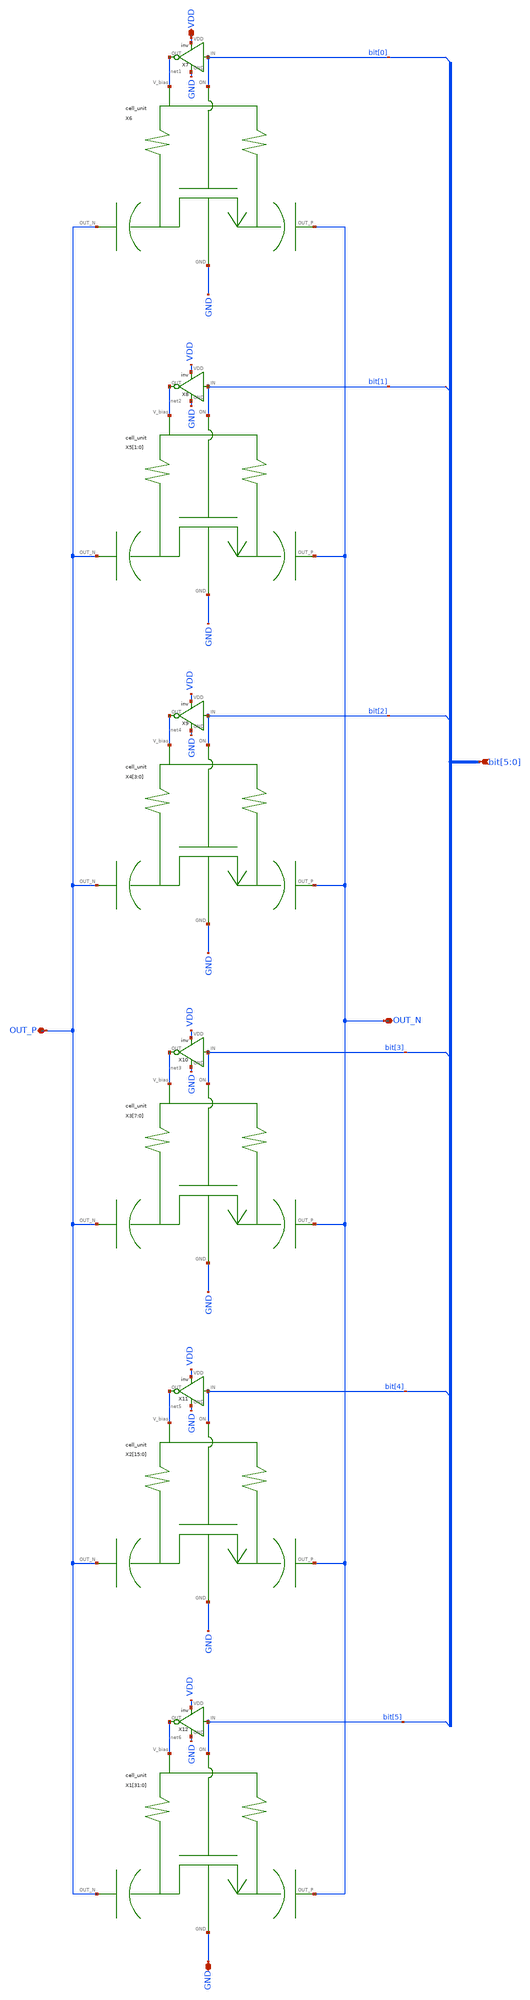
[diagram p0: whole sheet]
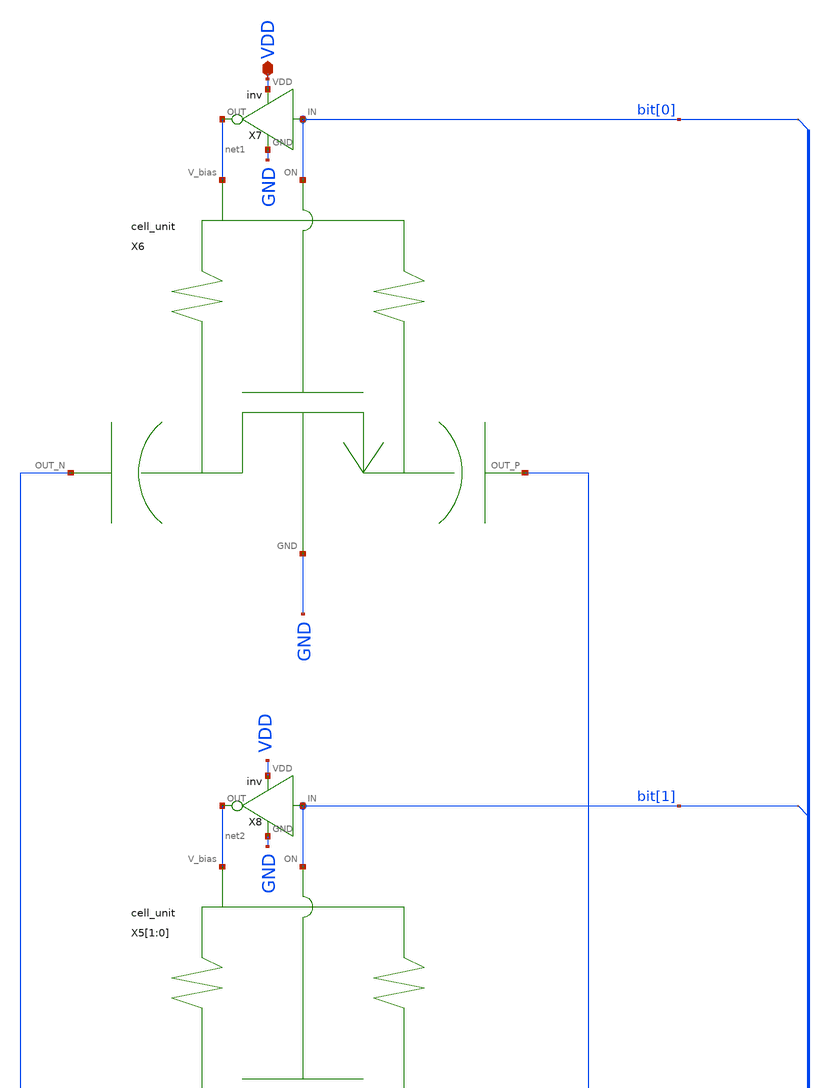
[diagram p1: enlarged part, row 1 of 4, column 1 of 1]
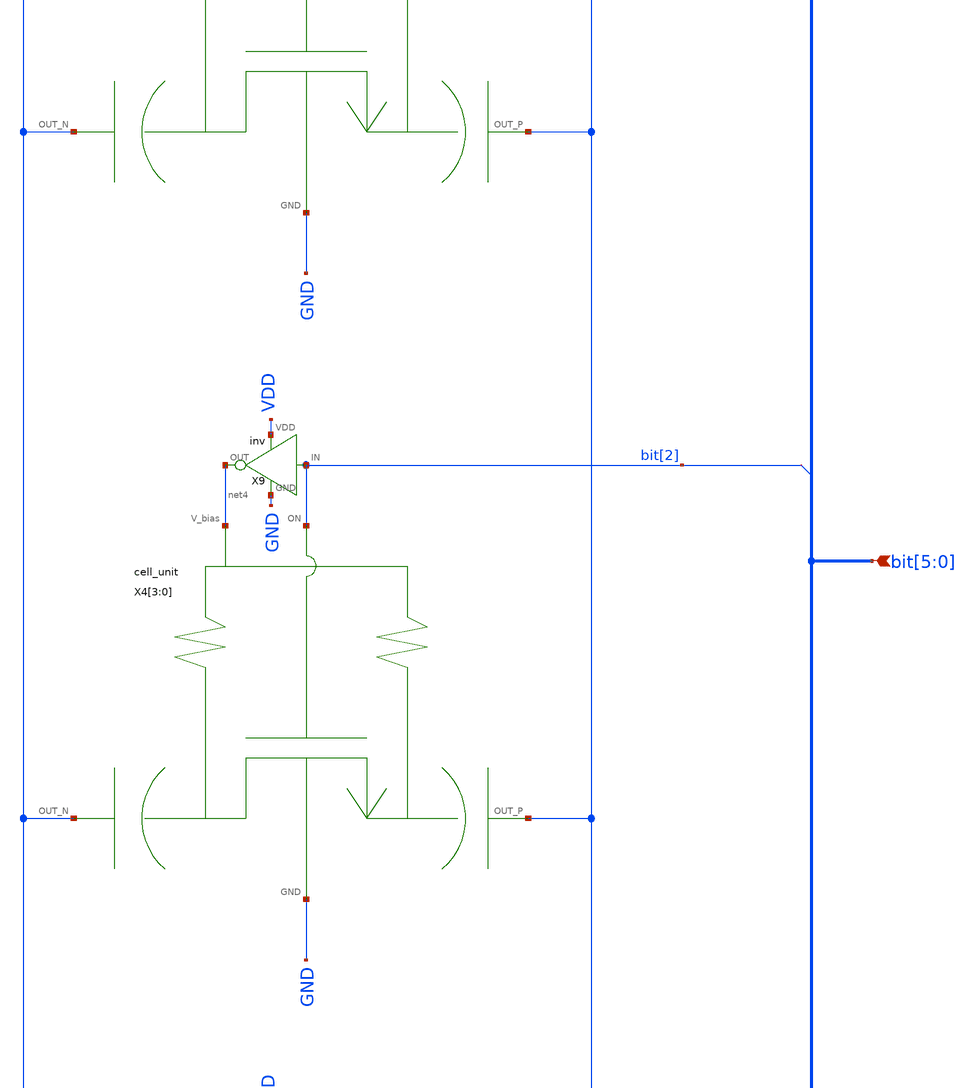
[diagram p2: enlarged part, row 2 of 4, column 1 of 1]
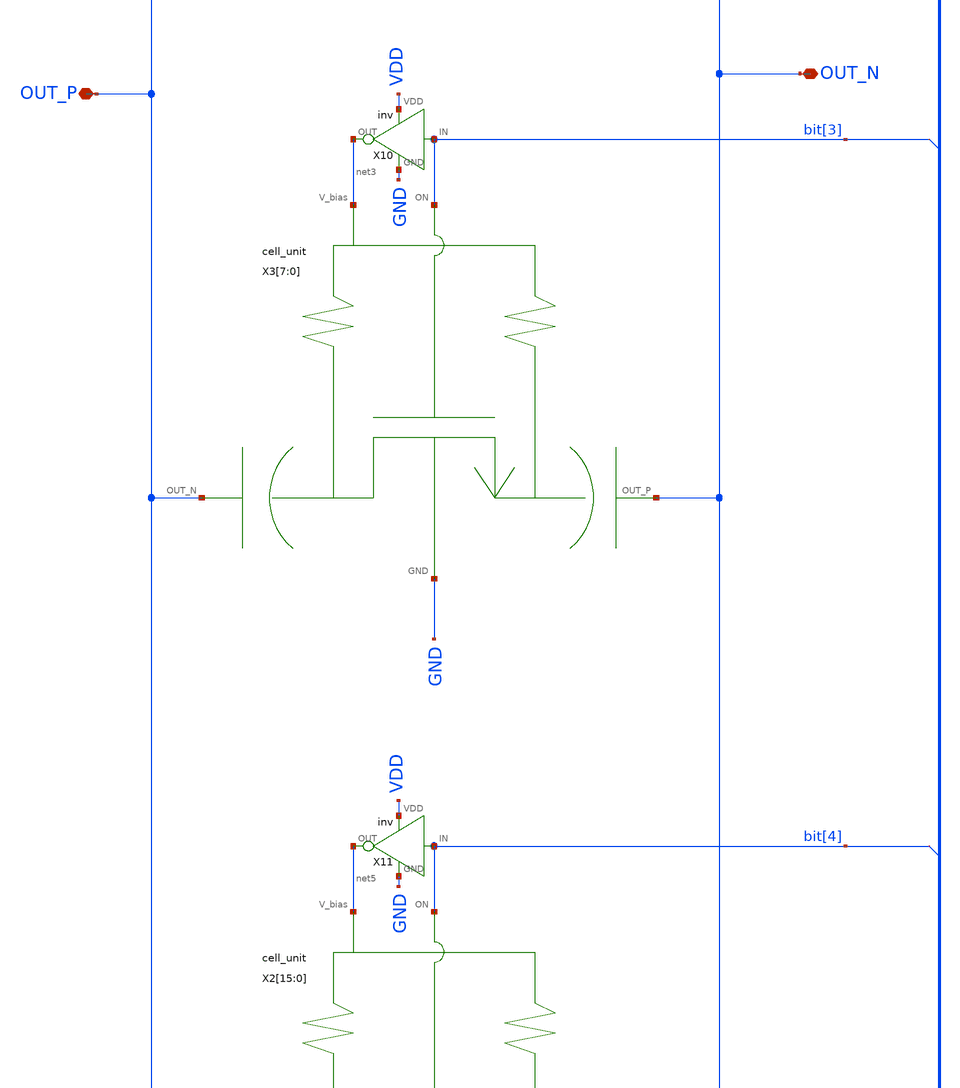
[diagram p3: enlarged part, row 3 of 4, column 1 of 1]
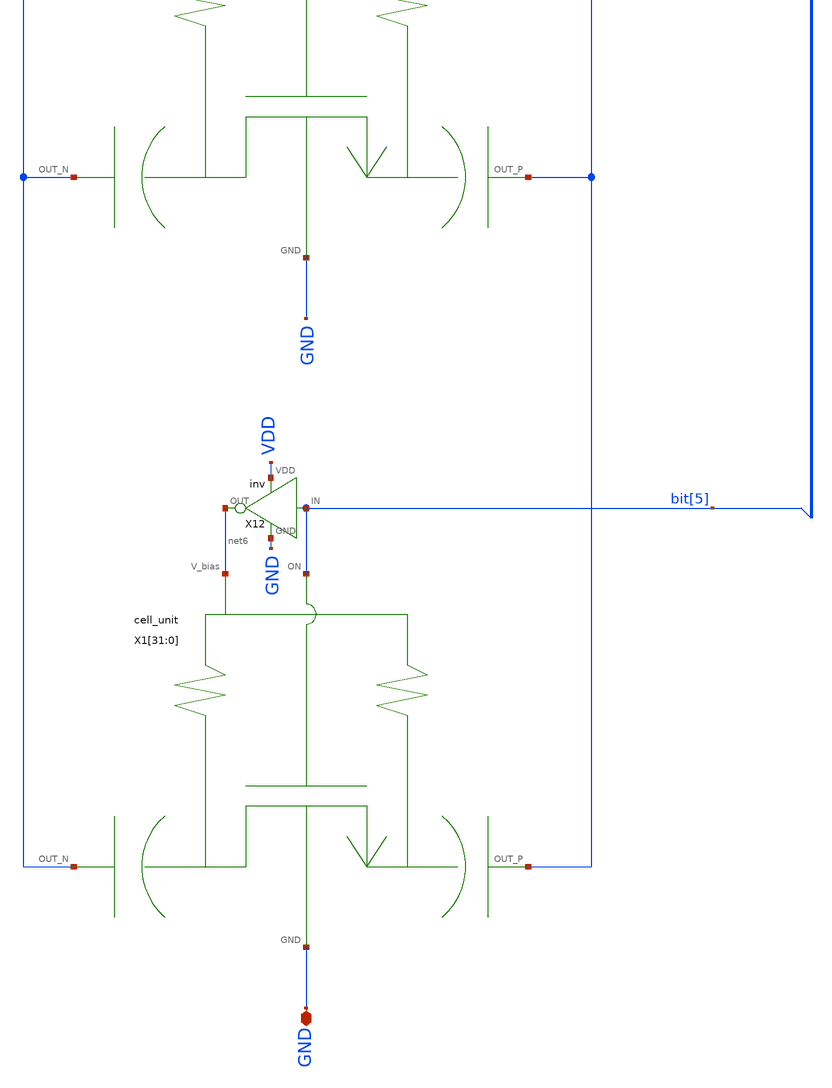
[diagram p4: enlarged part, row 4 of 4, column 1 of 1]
** sch_path: xschem/vco/parts/capbank.sch
**.subckt capbank VDD GND bit[5],bit[4],bit[3],bit[2],bit[1],bit[0] OUT_P OUT_N
*.iopin VDD
*.iopin GND
*.ipin bit[5],bit[4],bit[3],bit[2],bit[1],bit[0]
*.iopin OUT_P
*.iopin OUT_N
X1[31] net6 bit[5] OUT_P GND OUT_N cell_unit
X1[30] net6 bit[5] OUT_P GND OUT_N cell_unit
X1[29] net6 bit[5] OUT_P GND OUT_N cell_unit
X1[28] net6 bit[5] OUT_P GND OUT_N cell_unit
X1[27] net6 bit[5] OUT_P GND OUT_N cell_unit
X1[26] net6 bit[5] OUT_P GND OUT_N cell_unit
X1[25] net6 bit[5] OUT_P GND OUT_N cell_unit
X1[24] net6 bit[5] OUT_P GND OUT_N cell_unit
X1[23] net6 bit[5] OUT_P GND OUT_N cell_unit
X1[22] net6 bit[5] OUT_P GND OUT_N cell_unit
X1[21] net6 bit[5] OUT_P GND OUT_N cell_unit
X1[20] net6 bit[5] OUT_P GND OUT_N cell_unit
X1[19] net6 bit[5] OUT_P GND OUT_N cell_unit
X1[18] net6 bit[5] OUT_P GND OUT_N cell_unit
X1[17] net6 bit[5] OUT_P GND OUT_N cell_unit
X1[16] net6 bit[5] OUT_P GND OUT_N cell_unit
X1[15] net6 bit[5] OUT_P GND OUT_N cell_unit
X1[14] net6 bit[5] OUT_P GND OUT_N cell_unit
X1[13] net6 bit[5] OUT_P GND OUT_N cell_unit
X1[12] net6 bit[5] OUT_P GND OUT_N cell_unit
X1[11] net6 bit[5] OUT_P GND OUT_N cell_unit
X1[10] net6 bit[5] OUT_P GND OUT_N cell_unit
X1[9] net6 bit[5] OUT_P GND OUT_N cell_unit
X1[8] net6 bit[5] OUT_P GND OUT_N cell_unit
X1[7] net6 bit[5] OUT_P GND OUT_N cell_unit
X1[6] net6 bit[5] OUT_P GND OUT_N cell_unit
X1[5] net6 bit[5] OUT_P GND OUT_N cell_unit
X1[4] net6 bit[5] OUT_P GND OUT_N cell_unit
X1[3] net6 bit[5] OUT_P GND OUT_N cell_unit
X1[2] net6 bit[5] OUT_P GND OUT_N cell_unit
X1[1] net6 bit[5] OUT_P GND OUT_N cell_unit
X1[0] net6 bit[5] OUT_P GND OUT_N cell_unit
X2[15] net5 bit[4] OUT_P GND OUT_N cell_unit
X2[14] net5 bit[4] OUT_P GND OUT_N cell_unit
X2[13] net5 bit[4] OUT_P GND OUT_N cell_unit
X2[12] net5 bit[4] OUT_P GND OUT_N cell_unit
X2[11] net5 bit[4] OUT_P GND OUT_N cell_unit
X2[10] net5 bit[4] OUT_P GND OUT_N cell_unit
X2[9] net5 bit[4] OUT_P GND OUT_N cell_unit
X2[8] net5 bit[4] OUT_P GND OUT_N cell_unit
X2[7] net5 bit[4] OUT_P GND OUT_N cell_unit
X2[6] net5 bit[4] OUT_P GND OUT_N cell_unit
X2[5] net5 bit[4] OUT_P GND OUT_N cell_unit
X2[4] net5 bit[4] OUT_P GND OUT_N cell_unit
X2[3] net5 bit[4] OUT_P GND OUT_N cell_unit
X2[2] net5 bit[4] OUT_P GND OUT_N cell_unit
X2[1] net5 bit[4] OUT_P GND OUT_N cell_unit
X2[0] net5 bit[4] OUT_P GND OUT_N cell_unit
X3[7] net3 bit[3] OUT_P GND OUT_N cell_unit
X3[6] net3 bit[3] OUT_P GND OUT_N cell_unit
X3[5] net3 bit[3] OUT_P GND OUT_N cell_unit
X3[4] net3 bit[3] OUT_P GND OUT_N cell_unit
X3[3] net3 bit[3] OUT_P GND OUT_N cell_unit
X3[2] net3 bit[3] OUT_P GND OUT_N cell_unit
X3[1] net3 bit[3] OUT_P GND OUT_N cell_unit
X3[0] net3 bit[3] OUT_P GND OUT_N cell_unit
X4[3] net4 bit[2] OUT_P GND OUT_N cell_unit
X4[2] net4 bit[2] OUT_P GND OUT_N cell_unit
X4[1] net4 bit[2] OUT_P GND OUT_N cell_unit
X4[0] net4 bit[2] OUT_P GND OUT_N cell_unit
X5[1] net2 bit[1] OUT_P GND OUT_N cell_unit
X5[0] net2 bit[1] OUT_P GND OUT_N cell_unit
X6 net1 bit[0] OUT_P GND OUT_N cell_unit
X7 bit[0] net1 VDD GND inv
X8 bit[1] net2 VDD GND inv
X9 bit[2] net4 VDD GND inv
X10 bit[3] net3 VDD GND inv
X11 bit[4] net5 VDD GND inv
X12 bit[5] net6 VDD GND inv
**.ends
.end
